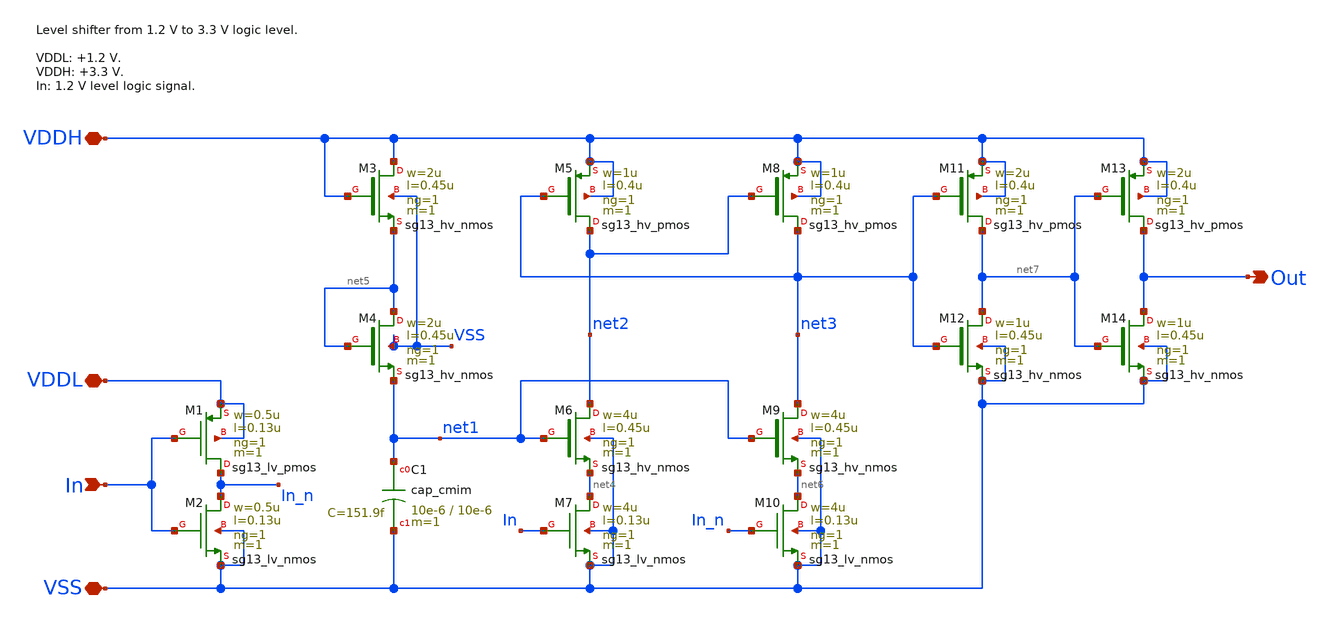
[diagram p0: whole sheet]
** sch_path: sar_adc/xschem/blocks/level_shifter/level_shifter.sch
**.subckt level_shifter In VSS Out VDDH VDDL
*.ipin In
*.iopin VSS
*.opin Out
*.iopin VDDH
*.iopin VDDL
XM5 net2 net3 VDDH VDDH sg13_hv_pmos w=1u l=0.4u ng=1 m=1 mm_ok=1
XM8 net3 net2 VDDH VDDH sg13_hv_pmos w=1u l=0.4u ng=1 m=1 mm_ok=1
XM7 net4 In VSS VSS sg13_lv_nmos w=4u l=0.13u ng=1 m=1 mm_ok=1
XM6 net2 net1 net4 VSS sg13_hv_nmos w=4u l=0.45u ng=1 m=1 mm_ok=1
XM3 VDDH VDDH net5 VSS sg13_hv_nmos w=2u l=0.45u ng=1 m=1 mm_ok=1
XM4 net5 net5 net1 VSS sg13_hv_nmos w=2u l=0.45u ng=1 m=1 mm_ok=1
XM9 net3 net1 net6 VSS sg13_hv_nmos w=4u l=0.45u ng=1 m=1 mm_ok=1
XM2 In_n In VSS VSS sg13_lv_nmos w=0.5u l=0.13u ng=1 m=1 mm_ok=1
XM1 In_n In VDDL VDDL sg13_lv_pmos w=0.5u l=0.13u ng=1 m=1 mm_ok=1
XM10 net6 In_n VSS VSS sg13_lv_nmos w=4u l=0.13u ng=1 m=1 mm_ok=1
XC1 net1 VSS cap_cmim w=10e-6 l=10e-6 m=1 mm_ok=1
XM11 net7 net3 VDDH VDDH sg13_hv_pmos w=2u l=0.4u ng=1 m=1 mm_ok=1
XM13 Out net7 VDDH VDDH sg13_hv_pmos w=2u l=0.4u ng=1 m=1 mm_ok=1
XM12 net7 net3 VSS VSS sg13_hv_nmos w=1u l=0.45u ng=1 m=1 mm_ok=1
XM14 Out net7 VSS VSS sg13_hv_nmos w=1u l=0.45u ng=1 m=1 mm_ok=1
**.ends
.end
